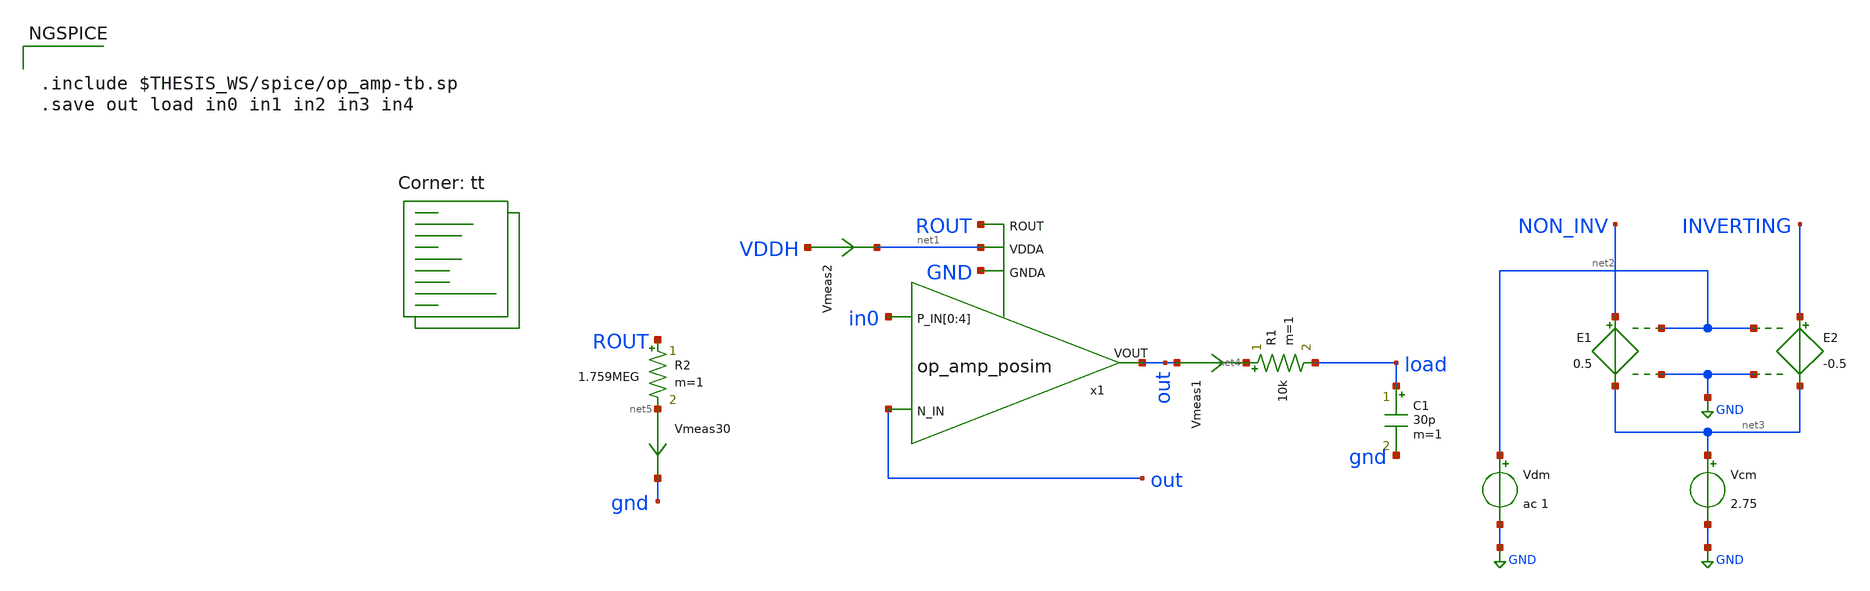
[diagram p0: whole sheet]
** sch_path: designs/libs/tb_analog/tb_two_stage_ota/op_amp_top-tb.sch
**.subckt op_amp_top-tb
C1 load gnd 30p m=1
Vmeas1 out net4 0
.save i(vmeas1)
Vmeas30 net5 gnd 0
.save i(vmeas30)
Vmeas2 VDDH net1 0
.save i(vmeas2)
E1 NON_INV net3 net2 GND 0.5
E2 INVERTING net3 net2 GND -0.5
Vdm net2 GND ac 1
Vcm net3 GND 2.75
R2 ROUT net5 1.759MEG m=1
R1 net4 load 10k m=1
x1 in0 in0 in0 in0 in0 out out ROUT net1 GND op_amp_posim
**** begin user architecture code


.include $THESIS_WS/spice/op_amp-tb.sp
.save out load in0 in1 in2 in3 in4


.lib $::SKYWATER_MODELS/sky130.lib.spice tt
**** end user architecture code
**.ends
.GLOBAL GND
.end
